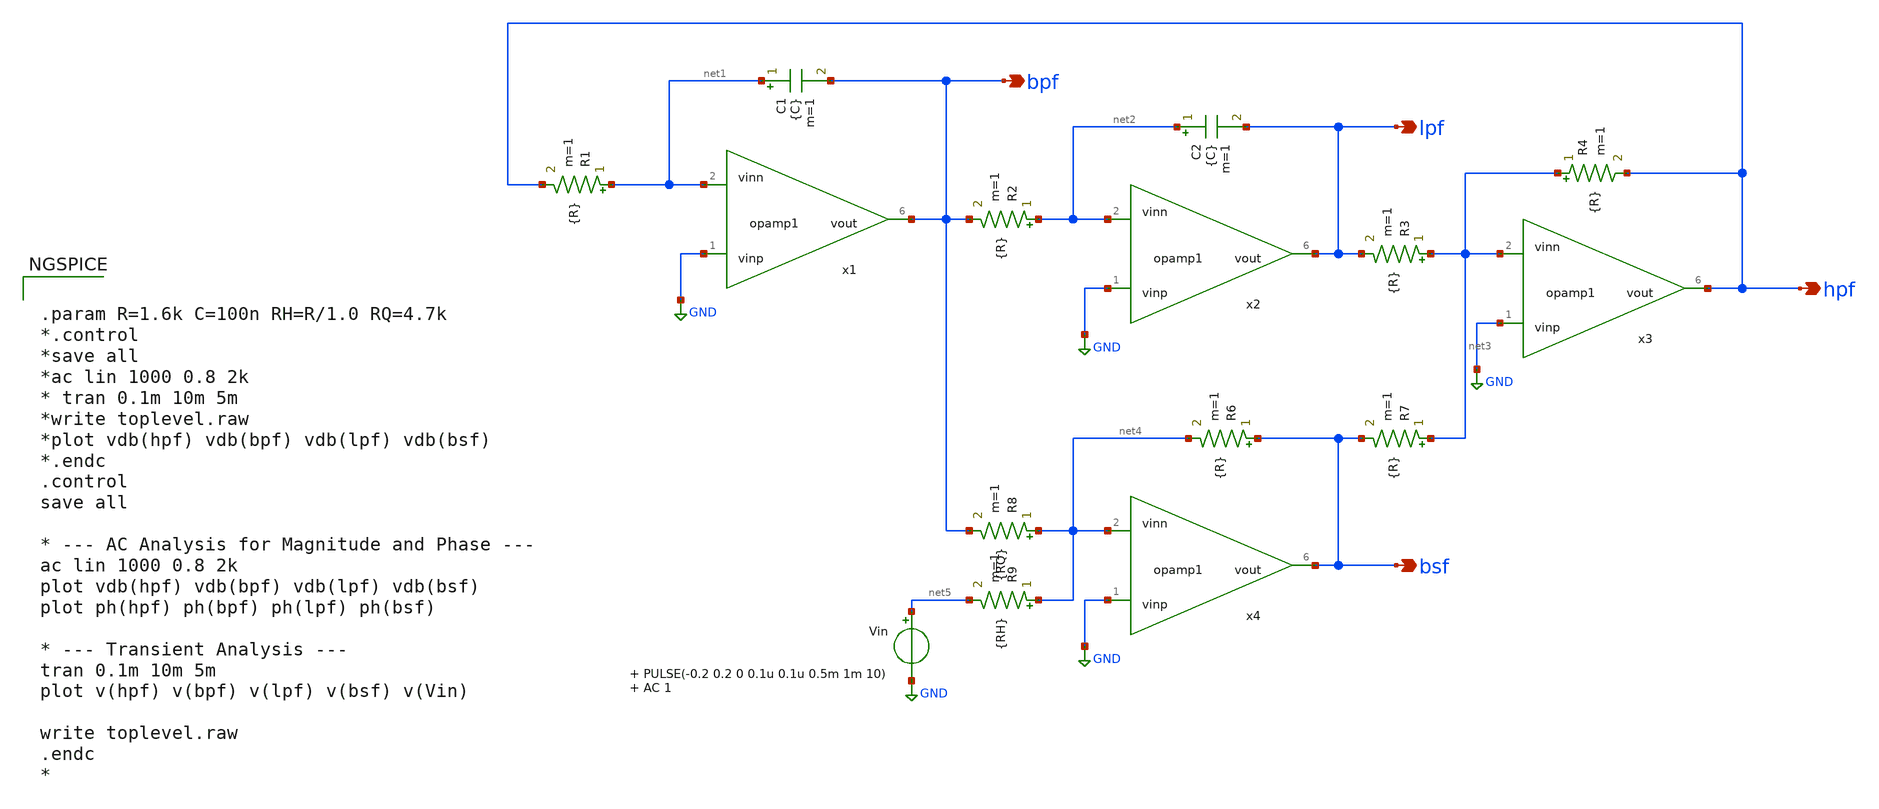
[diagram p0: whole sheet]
** sch_path: 2_Ideal_Cir/toplevel.sch
**.subckt toplevel bpf lpf hpf bsf
*.opin bpf
*.opin lpf
*.opin hpf
*.opin bsf
R1 net1 hpf {R} m=1
C1 net1 bpf {C} m=1
R2 net2 bpf {R} m=1
C2 net2 lpf {C} m=1
R3 net3 lpf {R} m=1
R4 net3 hpf {R} m=1
R6 bsf net4 {R} m=1
R7 net3 bsf {R} m=1
R8 net4 bpf {RQ} m=1
R9 net4 net5 {RH} m=1
Vin net5 GND PULSE(-0.2 0.2 0 0.1u 0.1u 0.5m 1m 10) AC 1

x1 GND net1 bpf opamp1
x2 GND net2 lpf opamp1
x3 GND net3 hpf opamp1
x4 GND net4 bsf opamp1
**** begin user architecture code


.param R=1.6k C=100n RH=R/1.0 RQ=4.7k
*.control
*save all
*ac lin 1000 0.8 2k
* tran 0.1m 10m 5m
*write toplevel.raw
*plot vdb(hpf) vdb(bpf) vdb(lpf) vdb(bsf)
*.endc
.control
save all

* --- AC Analysis for Magnitude and Phase ---
ac lin 1000 0.8 2k
plot vdb(hpf) vdb(bpf) vdb(lpf) vdb(bsf)
plot ph(hpf) ph(bpf) ph(lpf) ph(bsf)

* --- Transient Analysis ---
tran 0.1m 10m 5m
plot v(hpf) v(bpf) v(lpf) v(bsf) v(Vin)

write toplevel.raw
.endc
*

**** end user architecture code
**.ends

* expanding   symbol:  opamp1.sym # of pins=3
** sym_path: 2_Ideal_Cir/opamp1.sym
.include /foss/designs/amcd-lab/2_Ideal_Cir/opamp1.cir
.GLOBAL GND
.end
